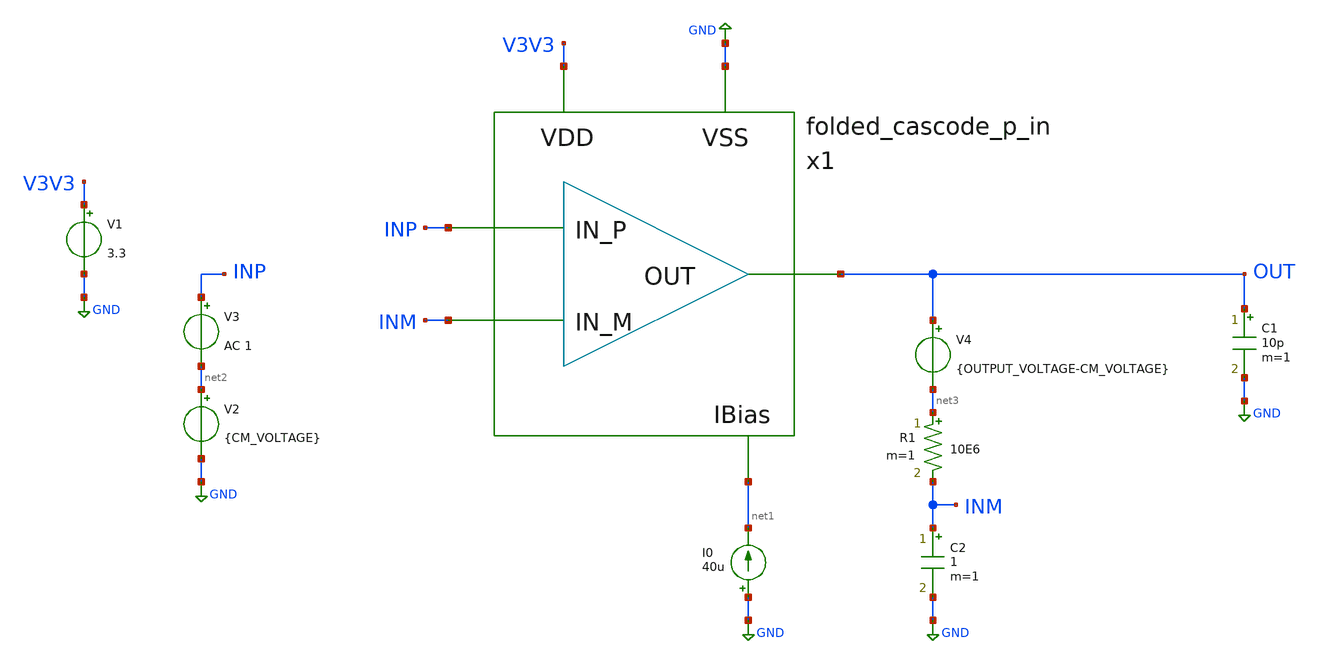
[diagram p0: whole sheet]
** sch_path: images/iic-osic-tools/addons/examples/open-pmic/design/folded-cascode-p-in/folded_cascode_p_in_tb.sch
**.subckt folded_cascode_p_in_tb
x1 INP INM OUT V3V3 GND net1 folded_cascode_p_in
V1 V3V3 GND 3.3
I0 GND net1 40u
V2 net2 GND {CM_VOLTAGE}
V3 INP net2 AC 1
C1 OUT GND 10p m=1
R1 net3 INM 10E6 m=1
V4 OUT net3 {OUTPUT_VOLTAGE-CM_VOLTAGE}
C2 INM GND 1 m=1
**** begin user architecture code

.lib $::SKYWATER_MODELS/models/sky130.lib.spice tt
.option wnflag=1



.param CM_VOLTAGE = 1.25
.param OUTPUT_VOLTAGE = 0.5
.control
save all
ac dec 200 10 1000Meg
settype decibel out
plot vdb(out)
let phase_val = 180/PI*cph(out)
let phase_margin_val = 180 + 180/PI*cph(out)
settype phase phase_val
plot phase_val
meas ac phase_margin find phase_margin_val when vdb(out)=0
meas ac crossover_freq WHEN vdb(out)=0
op
print v(inp)
print v(inm)
print v(out)
let v_offset = v(inp)-v(inm)
print v_offset
.endc


**** end user architecture code
**.ends
.GLOBAL GND
**** begin user architecture code
[sky130_models]
**** end user architecture code
.end
